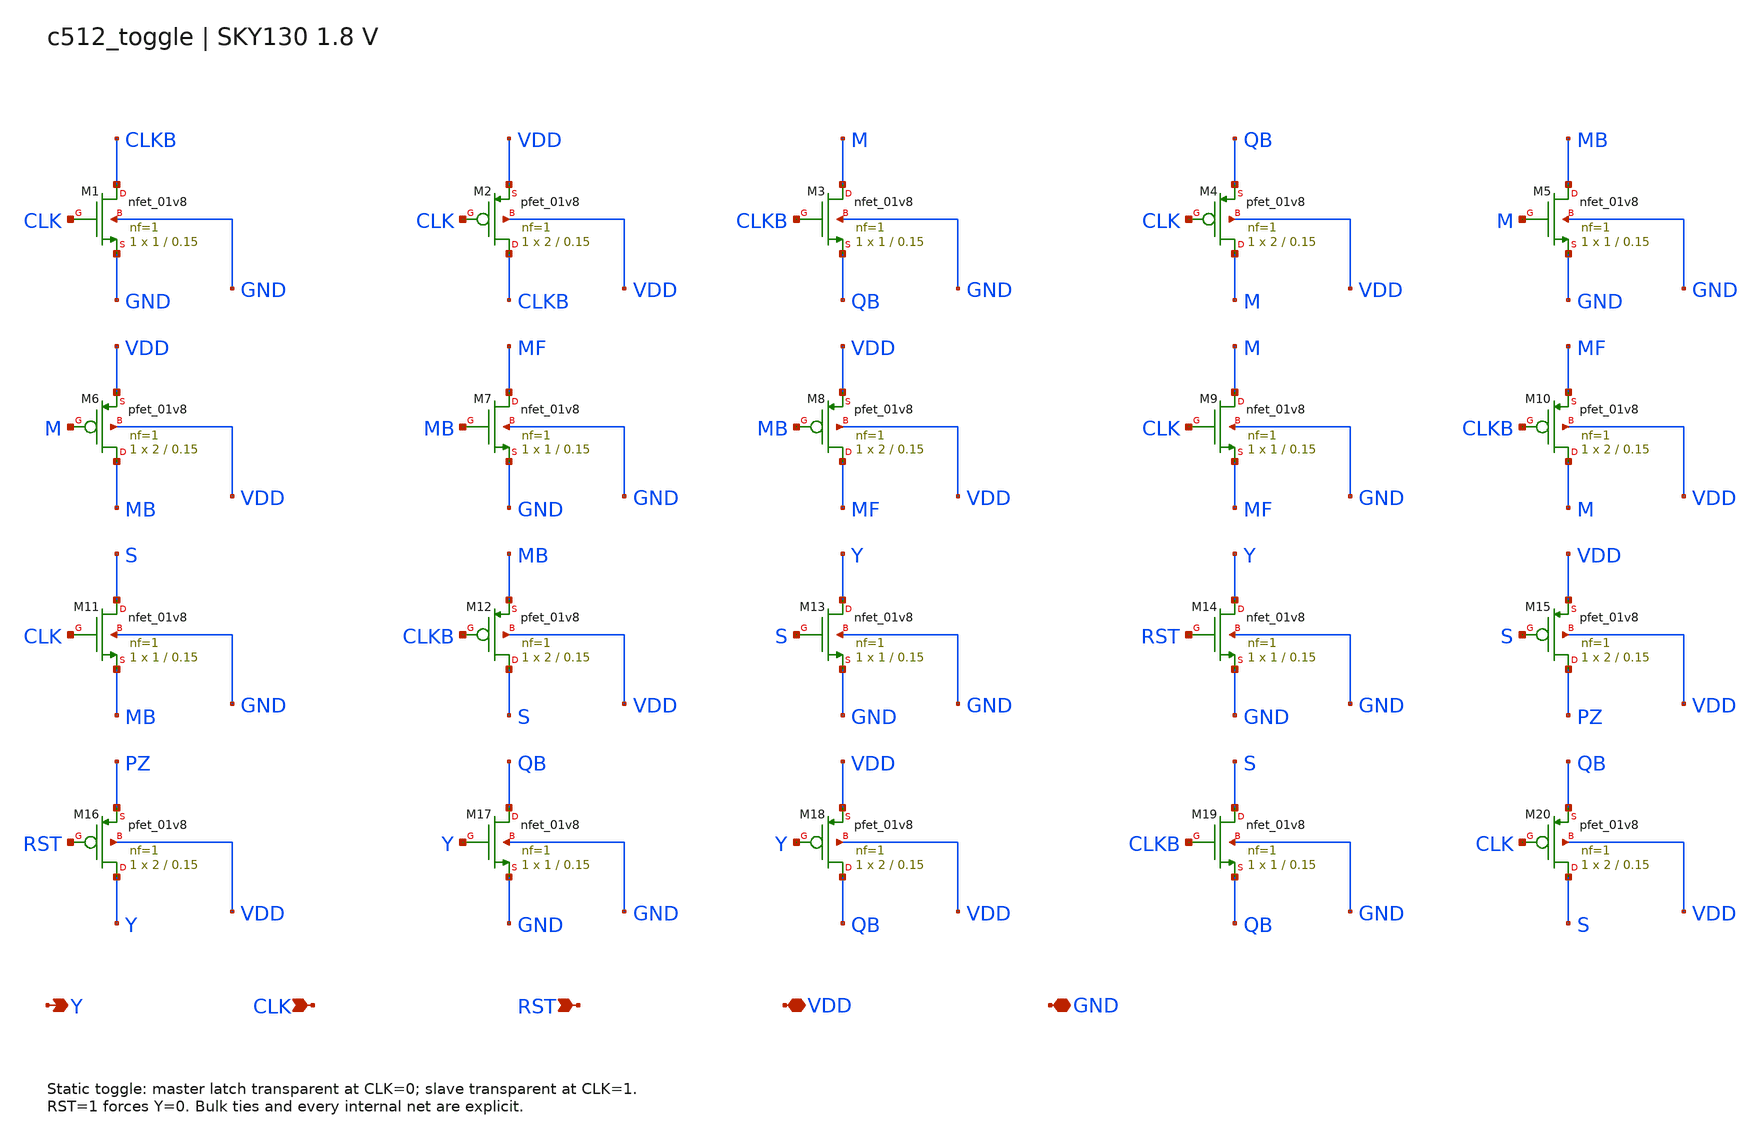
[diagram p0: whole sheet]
** sch_path: c512_toggle.sch
**.subckt c512_toggle Y CLK RST VDD GND
*.opin Y
*.ipin CLK
*.ipin RST
*.iopin VDD
*.iopin GND
XM1 CLKB CLK GND GND sky130_fd_pr__nfet_01v8 L=0.15 W=1 nf=1 ad=0.29 as=0.29 pd=2.58 ps=2.58
+ nrd=0.29 nrs=0.29 sa=0 sb=0 sd=0 mult=1 m=1
XM2 CLKB CLK VDD VDD sky130_fd_pr__pfet_01v8 L=0.15 W=2 nf=1 ad=0.58 as=0.58 pd=4.58 ps=4.58
+ nrd=0.145 nrs=0.145 sa=0 sb=0 sd=0 mult=1 m=1
XM3 M CLKB QB GND sky130_fd_pr__nfet_01v8 L=0.15 W=1 nf=1 ad=0.29 as=0.29 pd=2.58 ps=2.58 nrd=0.29
+ nrs=0.29 sa=0 sb=0 sd=0 mult=1 m=1
XM4 M CLK QB VDD sky130_fd_pr__pfet_01v8 L=0.15 W=2 nf=1 ad=0.58 as=0.58 pd=4.58 ps=4.58 nrd=0.145
+ nrs=0.145 sa=0 sb=0 sd=0 mult=1 m=1
XM5 MB M GND GND sky130_fd_pr__nfet_01v8 L=0.15 W=1 nf=1 ad=0.29 as=0.29 pd=2.58 ps=2.58 nrd=0.29
+ nrs=0.29 sa=0 sb=0 sd=0 mult=1 m=1
XM6 MB M VDD VDD sky130_fd_pr__pfet_01v8 L=0.15 W=2 nf=1 ad=0.58 as=0.58 pd=4.58 ps=4.58 nrd=0.145
+ nrs=0.145 sa=0 sb=0 sd=0 mult=1 m=1
XM7 MF MB GND GND sky130_fd_pr__nfet_01v8 L=0.15 W=1 nf=1 ad=0.29 as=0.29 pd=2.58 ps=2.58 nrd=0.29
+ nrs=0.29 sa=0 sb=0 sd=0 mult=1 m=1
XM8 MF MB VDD VDD sky130_fd_pr__pfet_01v8 L=0.15 W=2 nf=1 ad=0.58 as=0.58 pd=4.58 ps=4.58 nrd=0.145
+ nrs=0.145 sa=0 sb=0 sd=0 mult=1 m=1
XM9 M CLK MF GND sky130_fd_pr__nfet_01v8 L=0.15 W=1 nf=1 ad=0.29 as=0.29 pd=2.58 ps=2.58 nrd=0.29
+ nrs=0.29 sa=0 sb=0 sd=0 mult=1 m=1
XM10 M CLKB MF VDD sky130_fd_pr__pfet_01v8 L=0.15 W=2 nf=1 ad=0.58 as=0.58 pd=4.58 ps=4.58 nrd=0.145
+ nrs=0.145 sa=0 sb=0 sd=0 mult=1 m=1
XM11 S CLK MB GND sky130_fd_pr__nfet_01v8 L=0.15 W=1 nf=1 ad=0.29 as=0.29 pd=2.58 ps=2.58 nrd=0.29
+ nrs=0.29 sa=0 sb=0 sd=0 mult=1 m=1
XM12 S CLKB MB VDD sky130_fd_pr__pfet_01v8 L=0.15 W=2 nf=1 ad=0.58 as=0.58 pd=4.58 ps=4.58 nrd=0.145
+ nrs=0.145 sa=0 sb=0 sd=0 mult=1 m=1
XM13 Y S GND GND sky130_fd_pr__nfet_01v8 L=0.15 W=1 nf=1 ad=0.29 as=0.29 pd=2.58 ps=2.58 nrd=0.29
+ nrs=0.29 sa=0 sb=0 sd=0 mult=1 m=1
XM14 Y RST GND GND sky130_fd_pr__nfet_01v8 L=0.15 W=1 nf=1 ad=0.29 as=0.29 pd=2.58 ps=2.58 nrd=0.29
+ nrs=0.29 sa=0 sb=0 sd=0 mult=1 m=1
XM15 PZ S VDD VDD sky130_fd_pr__pfet_01v8 L=0.15 W=2 nf=1 ad=0.58 as=0.58 pd=4.58 ps=4.58 nrd=0.145
+ nrs=0.145 sa=0 sb=0 sd=0 mult=1 m=1
XM16 Y RST PZ VDD sky130_fd_pr__pfet_01v8 L=0.15 W=2 nf=1 ad=0.58 as=0.58 pd=4.58 ps=4.58 nrd=0.145
+ nrs=0.145 sa=0 sb=0 sd=0 mult=1 m=1
XM17 QB Y GND GND sky130_fd_pr__nfet_01v8 L=0.15 W=1 nf=1 ad=0.29 as=0.29 pd=2.58 ps=2.58 nrd=0.29
+ nrs=0.29 sa=0 sb=0 sd=0 mult=1 m=1
XM18 QB Y VDD VDD sky130_fd_pr__pfet_01v8 L=0.15 W=2 nf=1 ad=0.58 as=0.58 pd=4.58 ps=4.58 nrd=0.145
+ nrs=0.145 sa=0 sb=0 sd=0 mult=1 m=1
XM19 S CLKB QB GND sky130_fd_pr__nfet_01v8 L=0.15 W=1 nf=1 ad=0.29 as=0.29 pd=2.58 ps=2.58 nrd=0.29
+ nrs=0.29 sa=0 sb=0 sd=0 mult=1 m=1
XM20 S CLK QB VDD sky130_fd_pr__pfet_01v8 L=0.15 W=2 nf=1 ad=0.58 as=0.58 pd=4.58 ps=4.58 nrd=0.145
+ nrs=0.145 sa=0 sb=0 sd=0 mult=1 m=1
**.ends
.end
